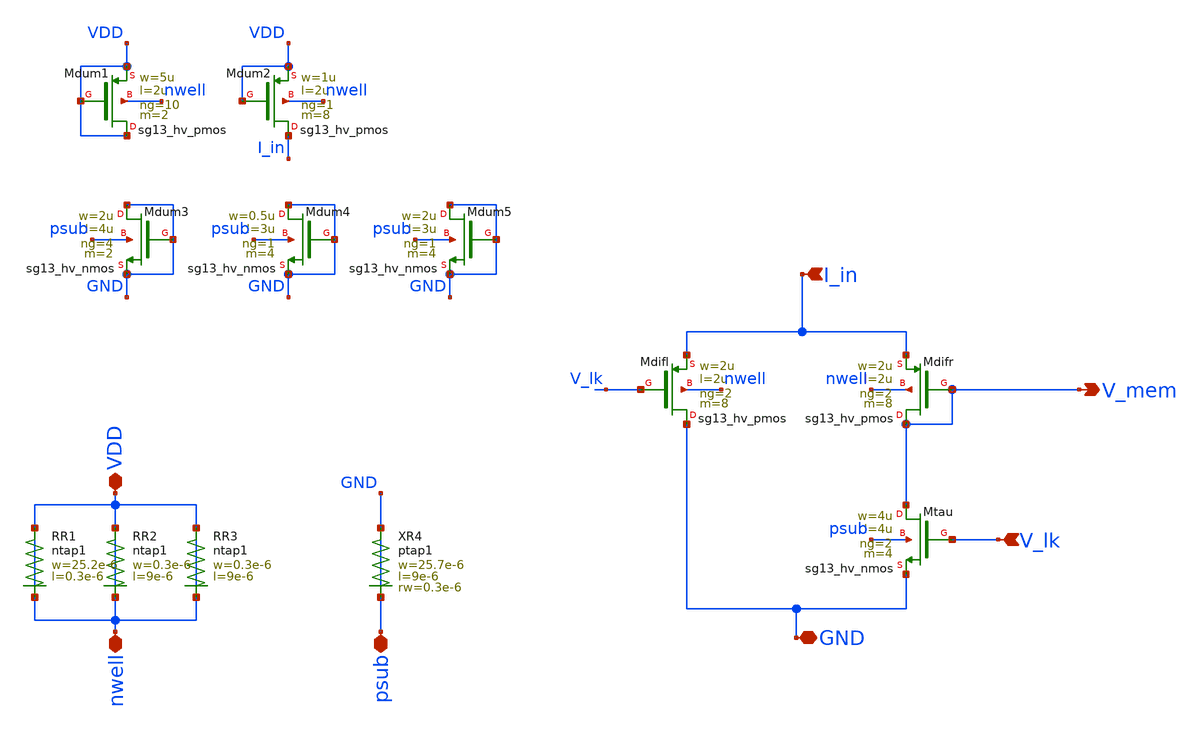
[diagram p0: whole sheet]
** sch_path: xschem/DPI_BK.sch
**.subckt DPI_BK V_mem V_lk I_in VDD GND nwell psub
*.opin V_mem
*.ipin V_lk
*.ipin I_in
*.iopin VDD
*.iopin GND
*.iopin nwell
*.iopin psub
XMdifl GND V_lk I_in nwell sg13_hv_pmos w=2u l=2u ng=2 m=8 mm_ok=1
XMdifr V_mem V_mem I_in nwell sg13_hv_pmos w=2u l=2u ng=2 m=8 mm_ok=1
XMtau V_mem V_lk GND psub sg13_hv_nmos w=4u l=4u ng=2 m=4 mm_ok=1
XR1 VDD VDD ntap1 R=16.73 w=25.2e-6 l=0.3e-6
XR2 VDD VDD ntap1 R=46.01 w=0.3e-6 l=9e-6
XR3 VDD VDD ntap1 R=46.01 w=0.3e-6 l=9e-6
XR4 psub psub ptap1 R=3.342 w=25.7e-6 l=9e-6 rw=0.3e-6
XMdum1 VDD VDD VDD nwell sg13_hv_pmos w=5u l=2u ng=10 m=2 mm_ok=1
XMdum2 I_in VDD VDD nwell sg13_hv_pmos w=1u l=2u ng=1 m=8 mm_ok=1
XMdum3 GND GND GND psub sg13_hv_nmos w=2u l=4u ng=4 m=2 mm_ok=1
XMdum4 GND GND GND psub sg13_hv_nmos w=0.5u l=3u ng=1 m=4 mm_ok=1
XMdum5 GND GND GND psub sg13_hv_nmos w=2u l=3u ng=1 m=4 mm_ok=1
**.ends
.end
